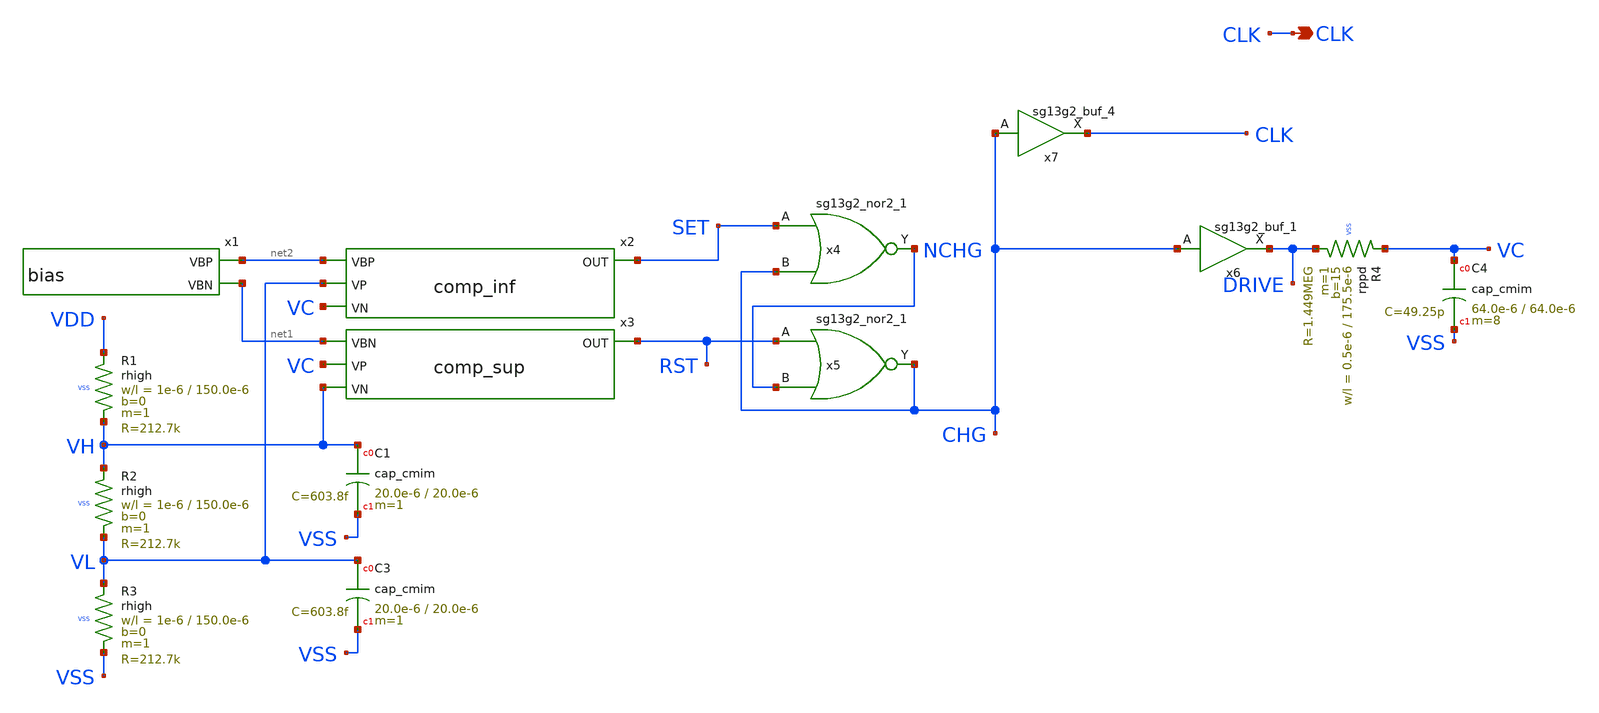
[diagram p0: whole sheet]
** sch_path: design/blocks/oscillator/schematic/wd_oscillater.sch
* IHP-GmbH/IHP-Open-PDK/ihp-sg13g2/libs.tech/xschem/sg13g2_stdcells/sg13g2_buf_1.sch:
* Copyright 2023 IHP PDK Authors
* Licensed under the Apache License, Version 2.0 (the "License");
**.subckt wd_oscillater CLK
*.opin CLK
x1 net2 net1 VDD VSS bias
x2 net2 VL VC SET VDD VSS comp_inf
x3 net1 VC VH RST VDD VSS comp_sup
XR1 VDD VH VSS rhigh w=1e-6 l=150.0e-6 m=1 b=0 mm_ok=1
XR2 VH VL VSS rhigh w=1e-6 l=150.0e-6 m=1 b=0 mm_ok=1
XR3 VL VSS VSS rhigh w=1e-6 l=150.0e-6 m=1 b=0 mm_ok=1
x4 NCHG SET CHG VDD VSS sg13g2_nor2_1
x5 CHG RST NCHG VDD VSS sg13g2_nor2_1
x6 DRIVE CHG VDD VSS sg13g2_buf_1
x7 CLK CHG VDD VSS sg13g2_buf_4
XR4 VC DRIVE VSS rppd w=0.5e-6 l=175.5e-6 m=1 b=15 mm_ok=1
XC1 VH VSS cap_cmim w=20.0e-6 l=20.0e-6 m=1 mm_ok=1
XC3 VL VSS cap_cmim w=20.0e-6 l=20.0e-6 m=1 mm_ok=1
XC4 VC VSS cap_cmim w=64.0e-6 l=64.0e-6 m=8 mm_ok=1
**.ends

* expanding   symbol:  bias.sym # of pins=2
** sym_path: design/blocks/bias/schematic/bias.sym
** sch_path: design/blocks/bias/schematic/bias.sch
.subckt bias VBP VBN VDD VSS
*.opin VBP
*.opin VBN
XM1 VBN VBN VSS VSS sg13_lv_nmos w=2u l=4u ng=1 m=1 mm_ok=1
XM2 VBP VBP VDD VDD sg13_lv_pmos w=4u l=4u ng=1 m=1 mm_ok=1
XR1 VDD VBN VSS rhigh w=0.5e-6 l=237.0e-6 m=1 b=0 mm_ok=1
XC1 VBN VSS cap_cmim w=26.0e-6 l=26.0e-6 m=1 mm_ok=1
XC2 VDD VBP cap_cmim w=26.0e-6 l=26.0e-6 m=1 mm_ok=1
XM3 VBP VBN VSS VSS sg13_lv_nmos w=2u l=4u ng=1 m=1 mm_ok=1
.ends


* expanding   symbol:  comp_inf.sym # of pins=4
** sym_path: design/blocks/comparator/schematic/comp_inf.sym
** sch_path: design/blocks/comparator/schematic/comp_inf.sch
.subckt comp_inf VBP VP VN OUT VDD VSS
*.opin OUT
*.ipin VN
*.ipin VP
*.ipin VBP
XM1 net3 VBP VDD VDD sg13_lv_pmos w=4u l=4u ng=1 m=1 mm_ok=1
XM7 net4 VP net3 VDD sg13_lv_pmos w=20u l=1u ng=4 m=1 mm_ok=1
XM8 net1 VN net3 VDD sg13_lv_pmos w=20u l=1u ng=4 m=1 mm_ok=1
XM9 net4 net4 VSS VSS sg13_lv_nmos w=1u l=8u ng=1 m=1 mm_ok=1
XM10 net1 net4 VSS VSS sg13_lv_nmos w=1u l=8u ng=1 m=1 mm_ok=1
XM2 net2 VBP VDD VDD sg13_lv_pmos w=4u l=4u ng=1 m=1 mm_ok=1
XM3 net2 net1 VSS VSS sg13_lv_nmos w=2u l=8u ng=1 m=1 mm_ok=1
x1 net2 OUT VDD VSS schmitt
.ends


* expanding   symbol:  comp_sup.sym # of pins=4
** sym_path: design/blocks/comparator/schematic/comp_sup.sym
** sch_path: design/blocks/comparator/schematic/comp_sup.sch
.subckt comp_sup VBN VP VN OUT VDD VSS
*.opin OUT
*.ipin VN
*.ipin VP
*.ipin VBN
XM2 net1 net1 VDD VDD sg13_lv_pmos w=2u l=4u ng=1 m=1 mm_ok=1
XM3 net3 net1 VDD VDD sg13_lv_pmos w=2u l=4u ng=1 m=1 mm_ok=1
XM4 net1 VP net2 VSS sg13_lv_nmos w=20u l=2u ng=4 m=1 mm_ok=1
XM5 net3 VN net2 VSS sg13_lv_nmos w=20u l=2u ng=4 m=1 mm_ok=1
XM6 net2 VBN VSS VSS sg13_lv_nmos w=2u l=4u ng=1 m=1 mm_ok=1
XM1 net4 net3 VDD VDD sg13_lv_pmos w=4u l=4u ng=1 m=1 mm_ok=1
XM7 net4 VBN VSS VSS sg13_lv_nmos w=2u l=4u ng=1 m=1 mm_ok=1
x1 net4 OUT VDD VSS schmitt
.ends


* expanding   symbol:  sg13g2_nor2_1.sym # of pins=3
** sym_path: sg13g2_nor2_1.sym
** sch_path: sg13g2_nor2_1.sch
.subckt sg13g2_nor2_1 Y A B VDD VSS
*.opin Y
*.ipin B
*.ipin A
*.iopin VDD
*.iopin VSS
XM1 Y A VSS VSS sg13_lv_nmos w=740.00n l=130.00n ng=1 m=1 mm_ok=1
XM2 Y B VSS VSS sg13_lv_nmos w=740.00n l=130.00n ng=1 m=1 mm_ok=1
XM3 net1 A VDD VDD sg13_lv_pmos w=1.12u l=130.00n ng=1 m=1 mm_ok=1
XM4 Y B net1 VDD sg13_lv_pmos w=1.12u l=130.00n ng=1 m=1 mm_ok=1
.ends


* expanding   symbol:  sg13g2_buf_1.sym # of pins=2
** sym_path: sg13g2_buf_1.sym
** sch_path: sg13g2_buf_1.sch
.subckt sg13g2_buf_1 X A VDD VSS
*.ipin A
*.opin X
*.iopin VDD
*.iopin VSS
XM1 net1 A VSS VSS sg13_lv_nmos w=550.00n l=130.00n ng=1 m=1 mm_ok=1
XM2 X net1 VSS VSS sg13_lv_nmos w=740.00n l=130.00n ng=1 m=1 mm_ok=1
XM3 net1 A VDD VDD sg13_lv_pmos w=840.00n l=130.00n ng=1 m=1 mm_ok=1
XM4 X net1 VDD VDD sg13_lv_pmos w=1.12u l=130.00n ng=1 m=1 mm_ok=1
.ends


* expanding   symbol:  sg13g2_buf_4.sym # of pins=2
** sym_path: sg13g2_buf_4.sym
** sch_path: sg13g2_buf_4.sch
.subckt sg13g2_buf_4 X A VDD VSS
*.ipin A
*.opin X
*.iopin VDD
*.iopin VSS
XM1 net1 A VSS VSS sg13_lv_nmos w=740.00n l=130.00n ng=1 m=1 mm_ok=1
XM2 X net1 VSS VSS sg13_lv_nmos w=2.96u l=130.00n ng=4 m=1 mm_ok=1
XM3 net1 A VDD VDD sg13_lv_pmos w=1.68u l=130.00n ng=2 m=1 mm_ok=1
XM4 X net1 VDD VDD sg13_lv_pmos w=4.48u l=130.00n ng=4 m=1 mm_ok=1
.ends


* expanding   symbol:  schmitt.sym # of pins=2
** sym_path: design/blocks/schmitt/schematic/schmitt.sym
** sch_path: design/blocks/schmitt/schematic/schmitt.sch
.subckt schmitt IN OUT VDD VSS
*.opin OUT
*.ipin IN
XM4 net1 IN VDD VDD sg13_lv_pmos w=1.04u l=0.13u ng=1 m=1 mm_ok=1
XM6 OUT IN net2 VSS sg13_lv_nmos w=0.76u l=0.13u ng=1 m=1 mm_ok=1
XM5 OUT IN net1 VDD sg13_lv_pmos w=1.04u l=0.13u ng=1 m=1 mm_ok=1
XM7 net2 IN VSS VSS sg13_lv_nmos w=0.76u l=0.13u ng=1 m=1 mm_ok=1
XM8 VSS OUT net1 VDD sg13_lv_pmos w=0.42u l=0.13u ng=1 m=1 mm_ok=1
XM9 VDD OUT net2 VSS sg13_lv_nmos w=0.42u l=0.13u ng=1 m=1 mm_ok=1
.ends

.end
